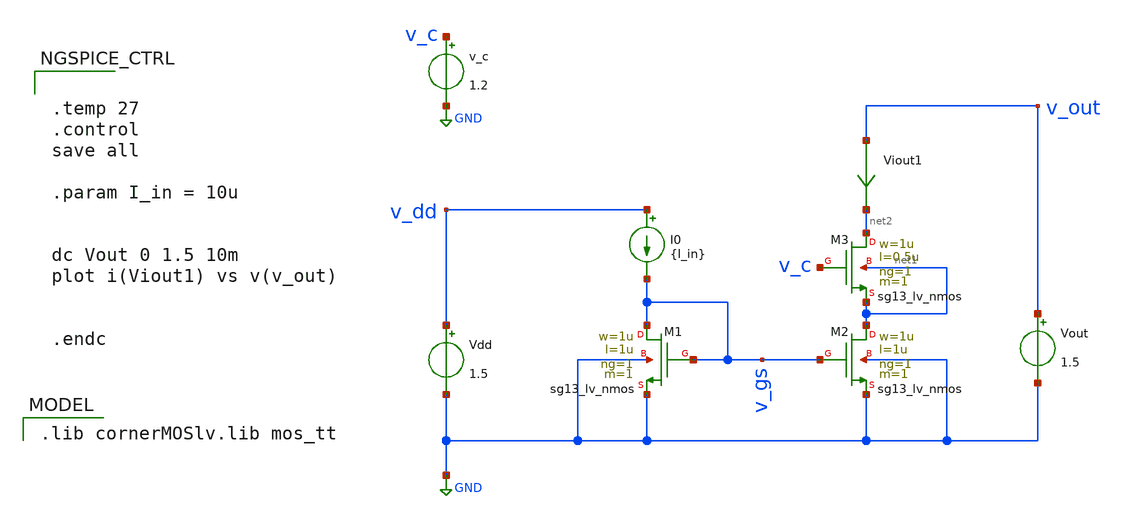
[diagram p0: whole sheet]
** sch_path: assignment_1_task_3.sch
**.subckt assignment_1_task_3
XM1 v_gs v_gs GND GND sg13_lv_nmos w=1u l=1u ng=1 m=1 mm_ok=1
XM2 net1 v_gs GND GND sg13_lv_nmos w=1u l=1u ng=1 m=1 mm_ok=1
Vdd v_dd GND 1.5
I0 v_dd v_gs {I_in}
Vout v_out GND 1.5
Viout1 v_out net2 0
.save i(viout1)
XM3 net2 v_c net1 net1 sg13_lv_nmos w=1u l=0.5u ng=1 m=1 mm_ok=1
v_c v_c GND 1.2
**** begin user architecture code


.temp 27
.control
save all

.param I_in = 10u


dc Vout 0 1.5 10m
plot i(Viout1) vs v(v_out)


.endc


 .lib cornerMOSlv.lib mos_tt

**** end user architecture code
**.ends
.GLOBAL GND
.end
